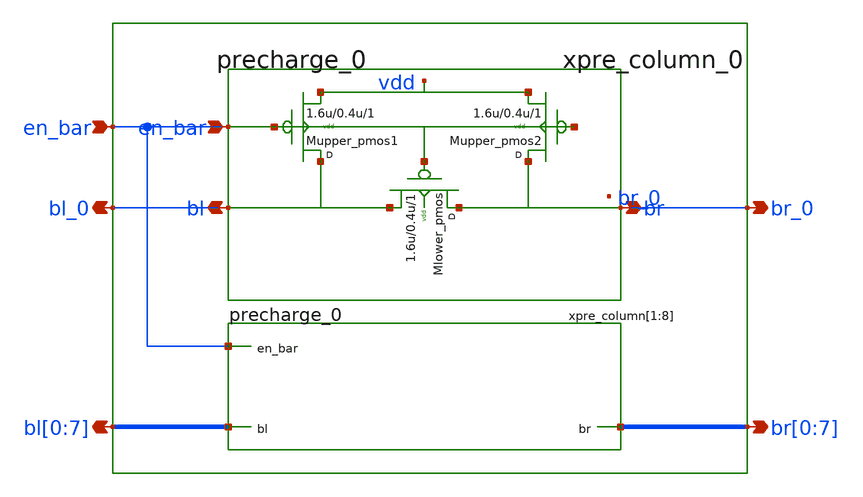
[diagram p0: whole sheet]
** sch_path: sram_2_64_scn4m_lcc/precharge_array.sch
**.subckt precharge_array bl_0 br_0 bl[0],bl[1],bl[2],bl[3],bl[4],bl[5],bl[6],bl[7]
*+ br[0],br[1],br[2],br[3],br[4],br[5],br[6],br[7] en_bar
*.opin bl_0
*.opin br_0
*.opin bl[0],bl[1],bl[2],bl[3],bl[4],bl[5],bl[6],bl[7]
*.opin br[0],br[1],br[2],br[3],br[4],br[5],br[6],br[7]
*.ipin en_bar
xpre_column[1] bl[0] br[0] en_bar vdd precharge_0
xpre_column[2] bl[1] br[1] en_bar vdd precharge_0
xpre_column[3] bl[2] br[2] en_bar vdd precharge_0
xpre_column[4] bl[3] br[3] en_bar vdd precharge_0
xpre_column[5] bl[4] br[4] en_bar vdd precharge_0
xpre_column[6] bl[5] br[5] en_bar vdd precharge_0
xpre_column[7] bl[6] br[6] en_bar vdd precharge_0
xpre_column[8] bl[7] br[7] en_bar vdd precharge_0
xpre_column_0 bl_0 br_0 en_bar vdd precharge_0
**.ends
.end
